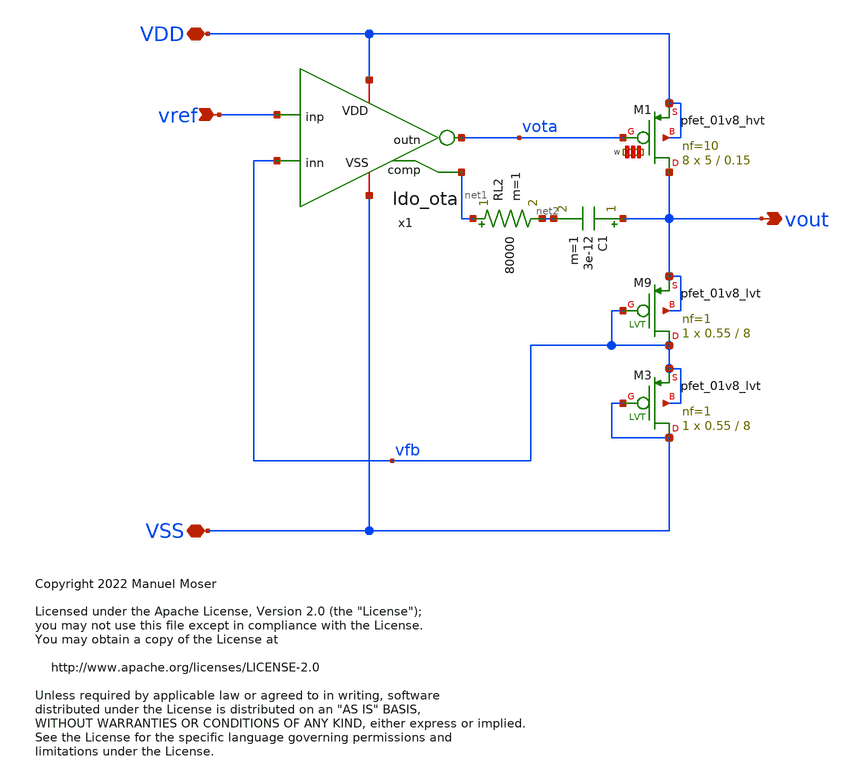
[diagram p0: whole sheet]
** sch_path: xschem/ldo.sch
* Copyright 2022 Manuel Moser
* Licensed under the Apache License, Version 2.0 (the "License");
**.subckt ldo vref VDD VSS vout
*.ipin vref
*.iopin VDD
*.iopin VSS
*.opin vout
x1 VDD vref vota vfb VSS net1 ldo_ota
XM1 vout vota VDD VDD sky130_fd_pr__pfet_01v8_hvt L=0.15 W='5 * 10 ' nf=10 ad='int((nf+1)/2) * W / nf * 0.29'
+ as='int((nf+2)/2) * W / nf * 0.29' pd='2*int((nf+1)/2) * (W / nf + 0.29)' ps='2*int((nf+2)/2) * (W / nf + 0.29)'
+ nrd='0.29 / W ' nrs='0.29 / W ' sa=0 sb=0 sd=0 mult=8 m=8
C1 vout net2 3e-12 m=1
RL2 net1 net2 80000 m=1
XM9 vfb vfb vout vout sky130_fd_pr__pfet_01v8_lvt L=8 W=0.55 nf=1 ad='int((nf+1)/2) * W/nf * 0.29' as='int((nf+2)/2) * W/nf * 0.29'
+ pd='2*int((nf+1)/2) * (W/nf + 0.29)' ps='2*int((nf+2)/2) * (W/nf + 0.29)' nrd='0.29 / W' nrs='0.29 / W'
+ sa=0 sb=0 sd=0 mult=1 m=1
XM3 VSS VSS vfb vfb sky130_fd_pr__pfet_01v8_lvt L=8 W=0.55 nf=1 ad='int((nf+1)/2) * W/nf * 0.29' as='int((nf+2)/2) * W/nf * 0.29'
+ pd='2*int((nf+1)/2) * (W/nf + 0.29)' ps='2*int((nf+2)/2) * (W/nf + 0.29)' nrd='0.29 / W' nrs='0.29 / W'
+ sa=0 sb=0 sd=0 mult=1 m=1
**.ends
.end
